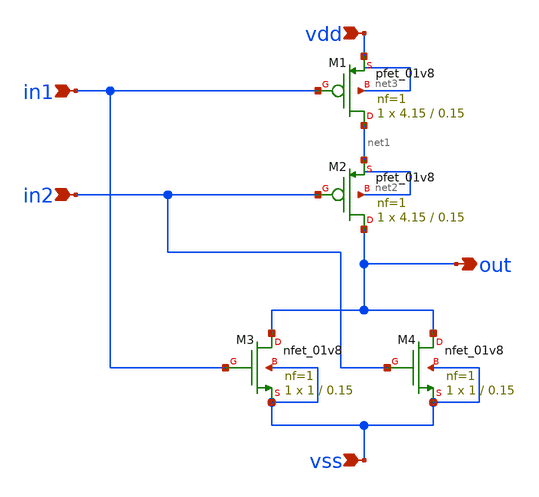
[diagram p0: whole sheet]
** sch_path: projects/carry_lookahead_adder/xschem/ports/nor.sch
**.subckt nor in1 in2 out vdd vss
*.ipin in1
*.ipin in2
*.opin out
*.ipin vdd
*.ipin vss
XM3 out in1 vss vss sky130_fd_pr__nfet_01v8 L=0.15 W=1 nf=1 ad='int((nf+1)/2) * W/nf * 0.29' as='int((nf+2)/2) * W/nf * 0.29'
+ pd='2*int((nf+1)/2) * (W/nf + 0.29)' ps='2*int((nf+2)/2) * (W/nf + 0.29)' nrd='0.29 / W' nrs='0.29 / W'
+ sa=0 sb=0 sd=0 mult=1 m=1
XM4 out in2 vss vss sky130_fd_pr__nfet_01v8 L=0.15 W=1 nf=1 ad='int((nf+1)/2) * W/nf * 0.29' as='int((nf+2)/2) * W/nf * 0.29'
+ pd='2*int((nf+1)/2) * (W/nf + 0.29)' ps='2*int((nf+2)/2) * (W/nf + 0.29)' nrd='0.29 / W' nrs='0.29 / W'
+ sa=0 sb=0 sd=0 mult=1 m=1
XM1 net1 in1 vdd net3 sky130_fd_pr__pfet_01v8 L=0.15 W=4.15 nf=1 ad='int((nf+1)/2) * W/nf * 0.29' as='int((nf+2)/2) * W/nf * 0.29'
+ pd='2*int((nf+1)/2) * (W/nf + 0.29)' ps='2*int((nf+2)/2) * (W/nf + 0.29)' nrd='0.29 / W' nrs='0.29 / W'
+ sa=0 sb=0 sd=0 mult=1 m=1
XM2 out in2 net1 net2 sky130_fd_pr__pfet_01v8 L=0.15 W=4.15 nf=1 ad='int((nf+1)/2) * W/nf * 0.29' as='int((nf+2)/2) * W/nf * 0.29'
+ pd='2*int((nf+1)/2) * (W/nf + 0.29)' ps='2*int((nf+2)/2) * (W/nf + 0.29)' nrd='0.29 / W' nrs='0.29 / W'
+ sa=0 sb=0 sd=0 mult=1 m=1
**.ends
.end
